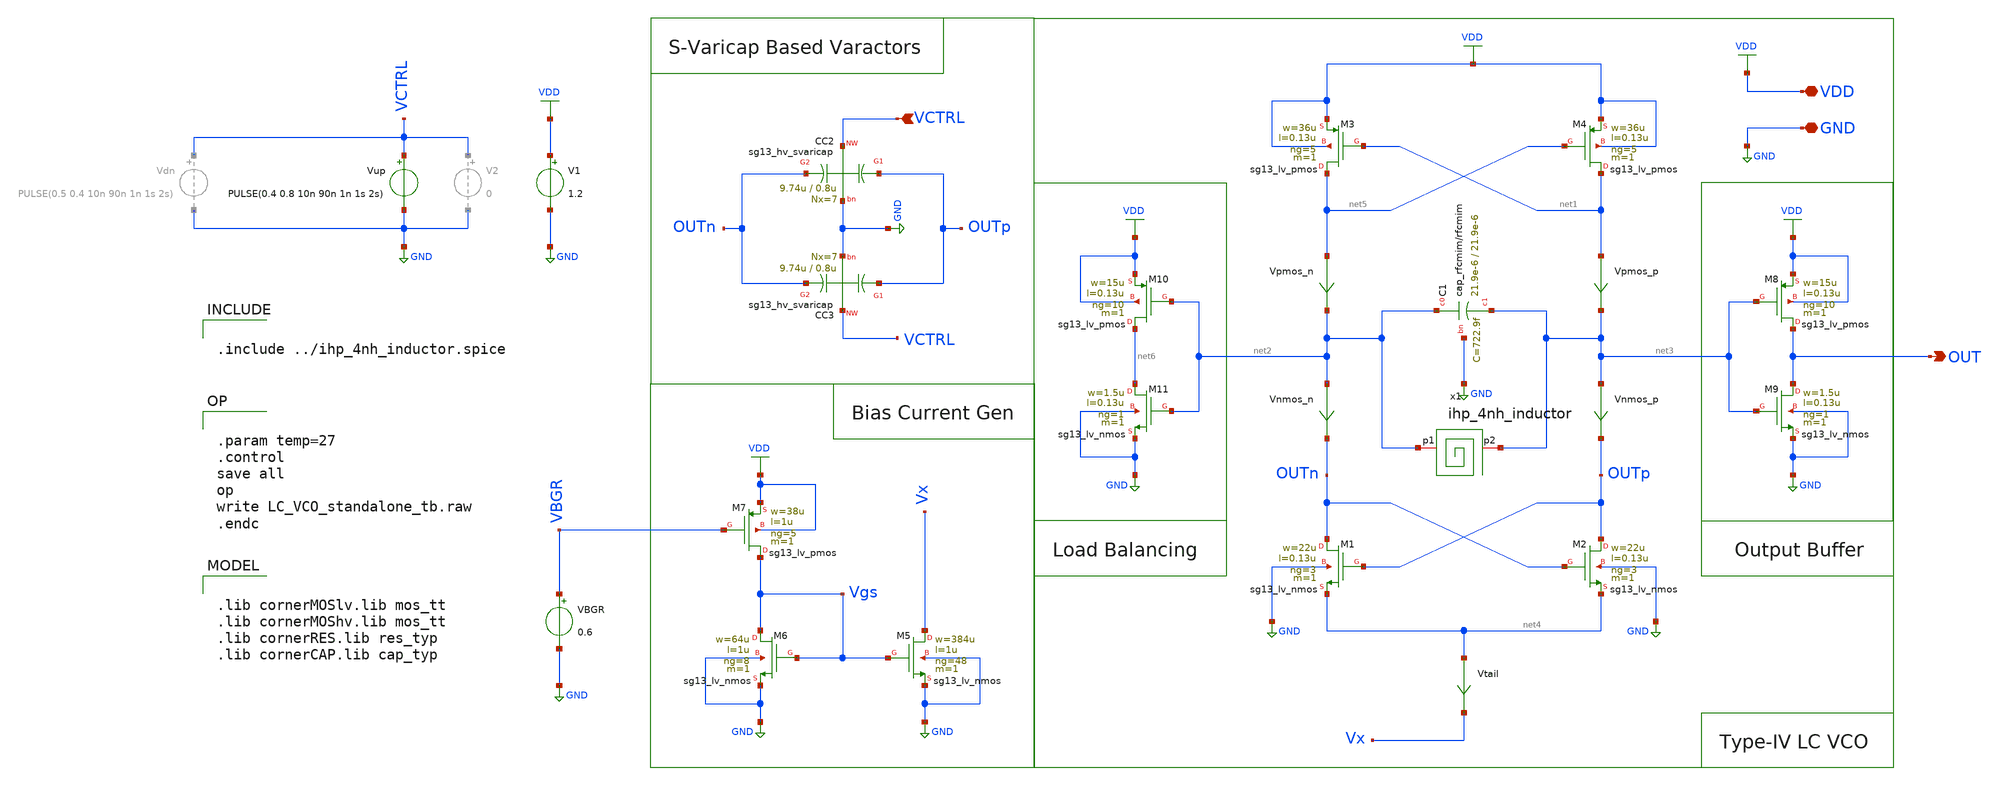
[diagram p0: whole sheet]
** sch_path: xschem/lc-vco/LC_VCO_standalone_tb.sch
**.subckt LC_VCO_standalone_tb OUT VCTRL VDD GND
*.opin OUT
*.ipin VCTRL
*.iopin VDD
*.iopin GND
XM5 Vx Vgs GND GND sg13_lv_nmos w=384u l=1u ng=48 m=1 mm_ok=1
XM4 net1 net5 VDD VDD sg13_lv_pmos w=36u l=0.13u ng=5 m=1 mm_ok=1
XM3 net5 net1 VDD VDD sg13_lv_pmos w=36u l=0.13u ng=5 m=1 mm_ok=1
XM2 OUTp OUTn net4 GND sg13_lv_nmos w=22u l=0.13u ng=3 m=1 mm_ok=1
XM1 OUTn OUTp net4 GND sg13_lv_nmos w=22u l=0.13u ng=3 m=1 mm_ok=1
Vpmos_p net1 net3 0
.save i(vpmos_p)
Vnmos_p net3 OUTp 0
.save i(vnmos_p)
Vtail net4 Vx 0
.save i(vtail)
XM6 Vgs Vgs GND GND sg13_lv_nmos w=64u l=1u ng=8 m=1 mm_ok=1
Vpmos_n net5 net2 0
.save i(vpmos_n)
Vnmos_n net2 OUTn 0
.save i(vnmos_n)
XC1 net2 net3 GND cap_rfcmim w=21.9e-6 l=21.9e-6 wfeed=10.0e-6 m=1 mm_ok=1
XC3 OUTp VCTRL OUTn GND sg13_hv_svaricap w=9.74u l=0.8u Nx=7
XC2 OUTp VCTRL OUTn GND sg13_hv_svaricap w=9.74u l=0.8u Nx=7
XM7 Vgs VBGR VDD VDD sg13_lv_pmos w=38u l=1u ng=5 m=1 mm_ok=1
XM8 OUT net3 VDD VDD sg13_lv_pmos w=15u l=0.13u ng=10 m=1 mm_ok=1
XM9 OUT net3 GND GND sg13_lv_nmos w=1.5u l=0.13u ng=1 m=1 mm_ok=1
XM10 net6 net2 VDD VDD sg13_lv_pmos w=15u l=0.13u ng=10 m=1 mm_ok=1
XM11 net6 net2 GND GND sg13_lv_nmos w=1.5u l=0.13u ng=1 m=1 mm_ok=1
V1 VDD GND 1.2
Vup VCTRL GND PULSE(0.4 0.8 10n 90n 1n 1s 2s)
VBGR VBGR GND 0.6
x1 net2 net3 ihp_4nh_inductor
**** begin user architecture code


.param temp=27
.control
save all
op
write LC_VCO_standalone_tb.raw
.endc



.lib cornerMOSlv.lib mos_tt
.lib cornerMOShv.lib mos_tt
.lib cornerRES.lib res_typ
.lib cornerCAP.lib cap_typ


.include ../ihp_4nh_inductor.spice




.param temp = 27
.options method=gear
.options savecurrents
.options noacct

.control

* Save required signals
save v(OUTp) v(Vx) v(OUT)

* Long transient simulation
tran 10p 500n 100n

* Find average power dissipation
let tot_power = abs(v(vdd)*i(v1))
meas tran avg_power AVG tot_power FROM=400n TO=450n

* Plot steady-state waveform
let vout = v(OUT)
meas tran vout_pp PP vout FROM=400n TO=450n
plot v(OUTp) v(OUT) xlimit 400n 405n

* FFT analysis
setplot tran1
linearize vout
set specwindow=blackman
fft vout

* Plot FFT spectrum
let power_db = db(vout)
plot power_db xlimit 2.34G 2.54G ylimit -200 0

* Find the maximum magnitude value between 2G and 3G
meas sp max_power_db max power_db FROM=2G TO=3G

.endc






.param temp = 27
.options method=gear
.options savecurrents
.options noacct

.control

* Save required signals
save v(OUTp) v(Vx)

* Long transient simulation
tran 10p 50n

* Plot transient waveform
plot v(OUTp) v(Vctrl) v(Vx) v(OUT)

* Find average power dissipation
let tot_power = abs(v(vdd)*i(v1))
plot tot_power xlimit 20n 35n

.endc



**** end user architecture code
**.ends
.GLOBAL GND
.GLOBAL VDD
.end
